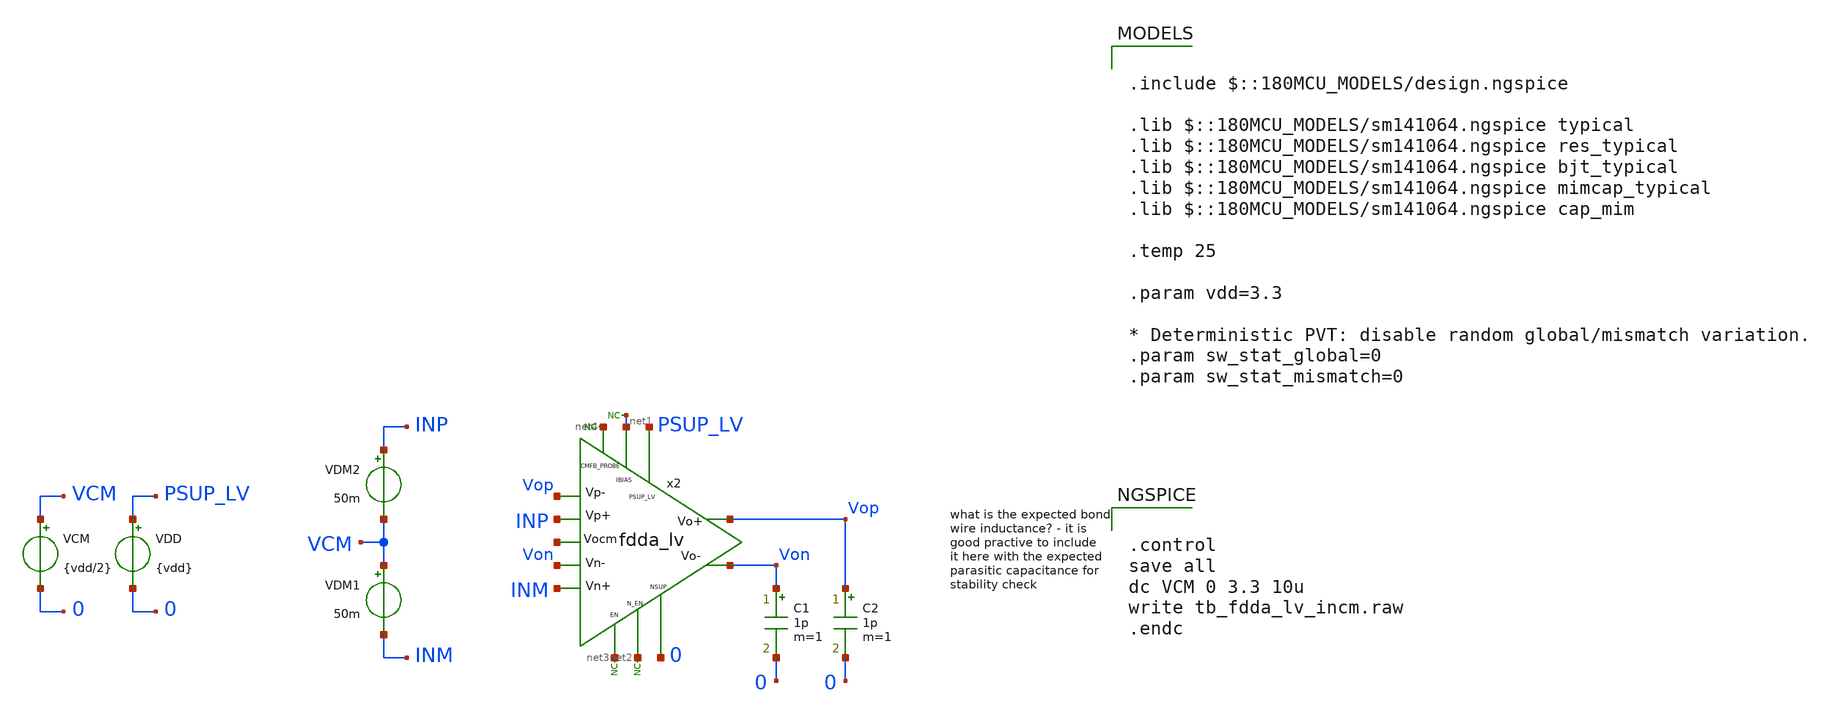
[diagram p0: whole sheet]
** sch_path: xschem/blocks/fdda_lv/tb_fdda_lv_incm.sch
**.subckt tb_fdda_lv_incm
C1 Von 0 1p m=1
x2 PSUP_LV Vop Von INM INP Vop Von net1 net2 net3 0 net4 net5 fdda_lv
* noconn #net1
* noconn #net3
* noconn #net2
VDD PSUP_LV 0 {vdd}
C2 Vop 0 1p m=1
VCM VCM 0 {vdd/2}
VDM2 INP VCM 50m
VDM1 VCM INM 50m
* noconn #net4
**** begin user architecture code

.include $::180MCU_MODELS/design.ngspice

.lib $::180MCU_MODELS/sm141064.ngspice typical
.lib $::180MCU_MODELS/sm141064.ngspice res_typical
.lib $::180MCU_MODELS/sm141064.ngspice bjt_typical
.lib $::180MCU_MODELS/sm141064.ngspice mimcap_typical
.lib $::180MCU_MODELS/sm141064.ngspice cap_mim

.temp 25

.param vdd=3.3

* Deterministic PVT: disable random global/mismatch variation.
.param sw_stat_global=0
.param sw_stat_mismatch=0



.control
save all
dc VCM 0 3.3 10u
write tb_fdda_lv_incm.raw
.endc


**** end user architecture code
**.ends
.end
